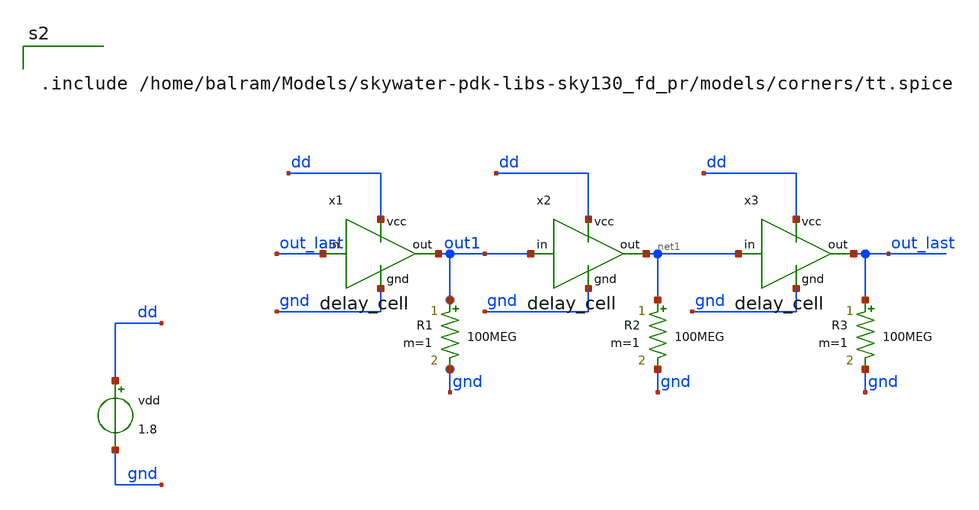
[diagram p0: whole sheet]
** sch_path: Oscillators/Ring-Oscillator/TB__oscillator.sch
**.subckt TB__oscillator
x1 dd out_last out1 gnd delay_cell
vdd dd gnd 1.8
x2 dd out1 net1 gnd delay_cell
x3 dd net1 out_last gnd delay_cell
R1 out1 gnd 100MEG m=1
R2 net1 gnd 100MEG m=1
R3 out_last gnd 100MEG m=1
**** begin user architecture code


.include /home/balram/Models/skywater-pdk-libs-sky130_fd_pr/models/corners/tt.spice


**** end user architecture code
**.ends

* expanding   symbol:  delay_cell.sym # of pins=4
** sym_path: Oscillators/Ring-Oscillator/delay_cell.sym
** sch_path: Oscillators/Ring-Oscillator/delay_cell.sch
.subckt delay_cell vcc in out gnd
*.ipin vcc
*.ipin gnd
*.ipin in
*.opin out
XM1 out in gnd gnd sky130_fd_pr__nfet_01v8_lvt L=0.15 W=0.45 nf=1 ad='int((1 + 1)/2) * 0.45 / 1 * 0.29'
+ as='int((1 + 2)/2) * 0.45 / 1 * 0.29' pd='2*int((1 + 1)/2) * (0.45 / 1 + 0.29)' ps='2*int((1 + 2)/2) * (0.45 / 1 + 0.29)'
+ nrd='0.29 / 0.45 ' nrs='0.29 / 0.45 ' sa=0 sb=0 sd=0 mult=1 m=1
XM10 out in vcc vcc sky130_fd_pr__pfet_01v8_lvt L=0.35 W=0.45 nf=1 ad='int((1 + 1)/2) * 0.45 / 1 * 0.29'
+ as='int((1 + 2)/2) * 0.45 / 1 * 0.29' pd='2*int((1 + 1)/2) * (0.45 / 1 + 0.29)' ps='2*int((1 + 2)/2) * (0.45 / 1 + 0.29)'
+ nrd='0.29 / 0.45 ' nrs='0.29 / 0.45 ' sa=0 sb=0 sd=0 mult=1 m=1
.ends

.end
